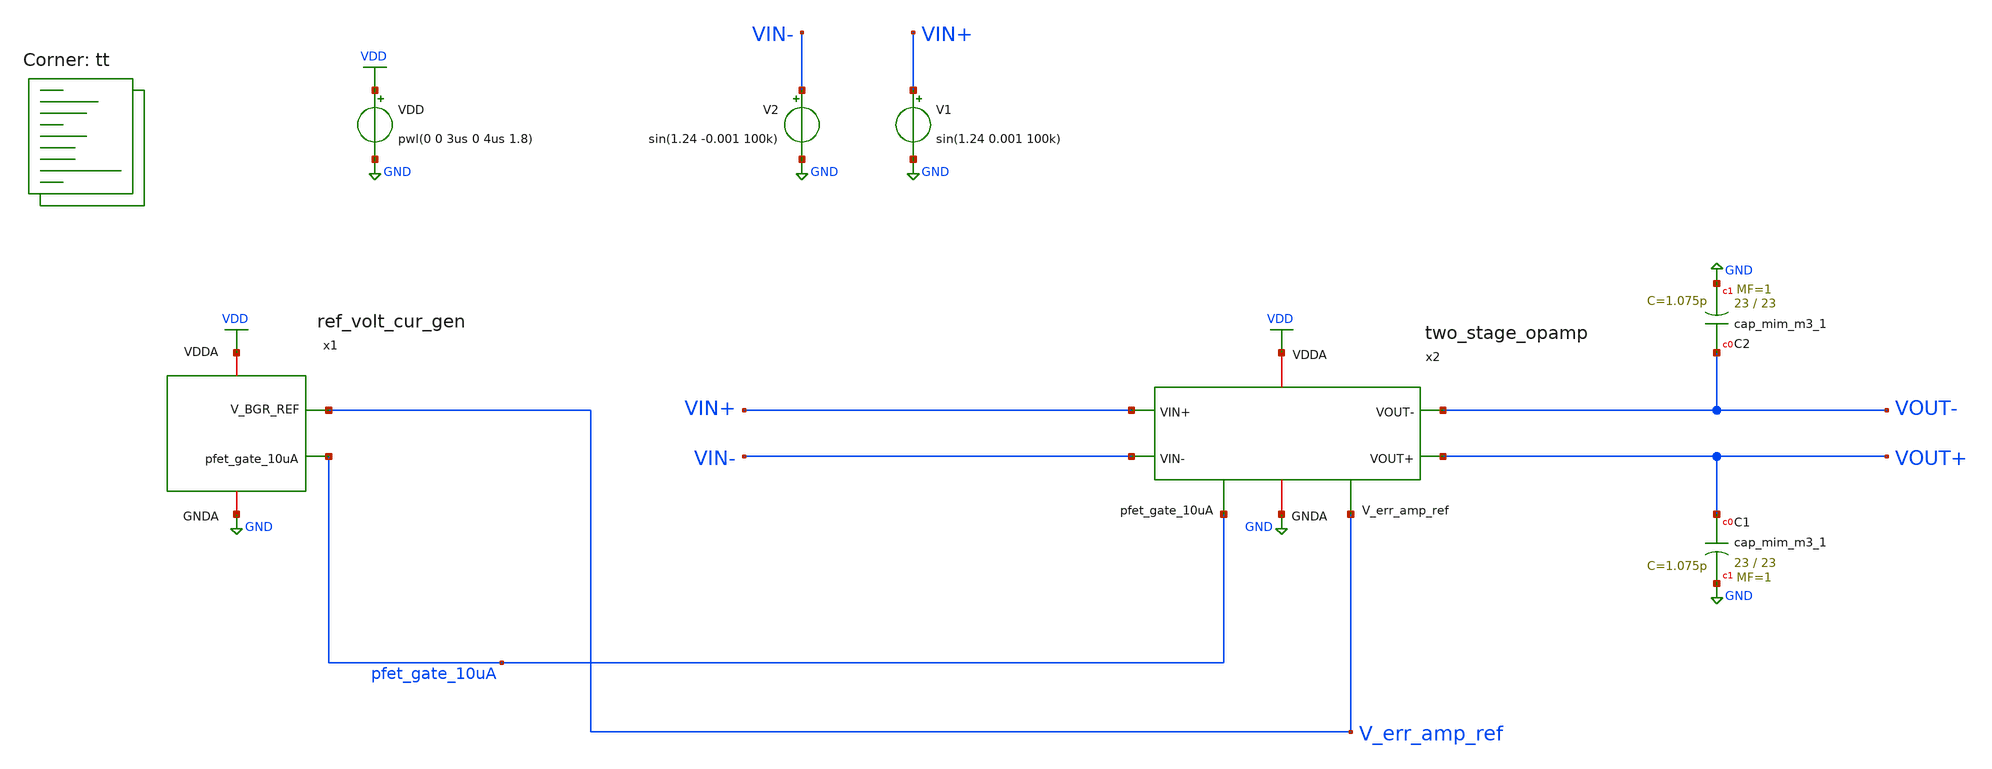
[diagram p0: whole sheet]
** sch_path: projects/opamp/xschem_ngspice/tb_opamp_full_6.sch
**.subckt tb_opamp_full_6
VDD VDD GND pwl(0 0 3us 0 4us 1.8)
V2 VIN- GND sin(1.24 -0.001 100k)
V1 VIN+ GND sin(1.24 0.001 100k)
x1 VDD V_err_amp_ref pfet_gate_10uA GND ref_volt_cur_gen
x2 VDD VOUT+ VOUT- pfet_gate_10uA V_err_amp_ref VIN+ VIN- GND two_stage_opamp
XC1 VOUT+ GND sky130_fd_pr__cap_mim_m3_1 W=23 L=23 MF=1 m=1
XC2 VOUT- GND sky130_fd_pr__cap_mim_m3_1 W=23 L=23 MF=1 m=1
**** begin user architecture code
.lib $::SKYWATER_MODELS/sky130.lib.spice tt




.option method=gear
.option wnflag=1
.option savecurrents

.save @m.x1.xm1.msky130_fd_pr__pfet_01v8[gm] @m.x1.xm1.msky130_fd_pr__pfet_01v8[vth] @m.x1.xm2.msky130_fd_pr__pfet_01v8[gm] @m.x1.xm2.msky130_fd_pr__pfet_01v8[vth] @m.x1.xm3.msky130_fd_pr__pfet_01v8[gm] @m.x1.xm3.msky130_fd_pr__pfet_01v8[vth] @m.x1.xm4.msky130_fd_pr__pfet_01v8[gm] @m.x1.xm4.msky130_fd_pr__pfet_01v8[vth] @m.x1.xm5.msky130_fd_pr__nfet_01v8[gm] @m.x1.xm5.msky130_fd_pr__nfet_01v8[vth] @m.x1.xm6.msky130_fd_pr__pfet_01v8[gm] @m.x1.xm6.msky130_fd_pr__pfet_01v8[vth] @m.x1.xm7.msky130_fd_pr__nfet_01v8[gm] @m.x1.xm7.msky130_fd_pr__nfet_01v8[vth] @m.x1.xm8.msky130_fd_pr__pfet_01v8[gm] @m.x1.xm8.msky130_fd_pr__pfet_01v8[vth] @m.x2.xm2.msky130_fd_pr__nfet_01v8[gm] @m.x2.xm2.msky130_fd_pr__nfet_01v8[vth] @m.x2.xm3.msky130_fd_pr__nfet_01v8[gm] @m.x2.xm3.msky130_fd_pr__nfet_01v8[vth] @m.x2.xm7.msky130_fd_pr__pfet_01v8[gm] @m.x2.xm7.msky130_fd_pr__pfet_01v8[vth] @m.x1.x1.xm1.msky130_fd_pr__nfet_01v8[gm] @m.x1.x1.xm2.msky130_fd_pr__nfet_01v8[gm] @m.x1.x1.xm3.msky130_fd_pr__nfet_01v8[gm] @m.x1.x1.xm4.msky130_fd_pr__nfet_01v8[gm] @m.x1.x1.xm5.msky130_fd_pr__pfet_01v8[gm] @m.x1.x1.xm6.msky130_fd_pr__nfet_01v8[gm] @m.x1.x1.xm7.msky130_fd_pr__pfet_01v8[gm] @m.x1.x2.xm1.msky130_fd_pr__nfet_01v8[gm] @m.x1.x2.xm2.msky130_fd_pr__nfet_01v8[gm] @m.x1.x2.xm3.msky130_fd_pr__nfet_01v8[gm] @m.x1.x2.xm4.msky130_fd_pr__nfet_01v8[gm] @m.x1.x2.xm5.msky130_fd_pr__pfet_01v8[gm] @m.x1.x2.xm6.msky130_fd_pr__nfet_01v8[gm] @m.x1.x2.xm7.msky130_fd_pr__pfet_01v8[gm] @m.x2.xm39.msky130_fd_pr__pfet_01v8[gm] @m.x2.xm39.msky130_fd_pr__pfet_01v8[vth] @m.x2.xm40.msky130_fd_pr__pfet_01v8[gm] @m.x2.xm40.msky130_fd_pr__pfet_01v8[vth]

* .ic v(v_top) = 1.8

.control

  * let runs=3
  * let run=1

  * dowhile run <= runs
    * save v(vout+) v(vout-) v(vin+) v(vin-) v(v_err_amp_ref) v(x2.x) v(x2.y) v(x2.vb1) v(x2.vb2)
+ v(x2.vb3) v(x2.v_tot)
    save all
    remzerovec
    set appendwrite
    * dc temp -40 120 10 VDD 0 4.0 0.2
    * dc VDD 0 2.0 0.02 temp -40 120 40
    * dc V5 0 0.01 0.0001
    tran 2n 30u
    * tran 1p 3n
    * tran 0.1ns 30us
    * ac dec 40 1 10T
    write tb_opamp_full_6.raw
    * write tb_opamp_full_6_mc.raw
    * write tb_opamp_full_6_tt_mm.raw
    * write tb_opamp_full_6_AC.raw
    * reset
    * let run = run + 1
  * end
.endc




**** end user architecture code
**.ends

* expanding   symbol:  ref_volt_cur_gen.sym # of pins=4
** sym_path: projects/opamp/xschem_ngspice/ref_volt_cur_gen.sym
** sch_path: projects/opamp/xschem_ngspice/ref_volt_cur_gen.sch
.subckt ref_volt_cur_gen VDDA V_BGR_REF pfet_gate_10uA GNDA
*.opin pfet_gate_10uA
*.iopin GNDA
*.opin V_BGR_REF
*.iopin VDDA
XM3 V_BGR_REF V_TOP VDDA VDDA sky130_fd_pr__pfet_01v8 L=0.5 W=10 nf=1 ad='int((nf+1)/2) * W/nf * 0.29'
+ as='int((nf+2)/2) * W/nf * 0.29' pd='2*int((nf+1)/2) * (W/nf + 0.29)' ps='2*int((nf+2)/2) * (W/nf + 0.29)'
+ nrd='0.29 / W' nrs='0.29 / W' sa=0 sb=0 sd=0 mult=1 m=1
XR4 GNDA V_BGR_REF GNDA sky130_fd_pr__res_xhigh_po_0p35 L=12.7 mult=1 m=1
XR5 GNDA V_CUR_REF_REG GNDA sky130_fd_pr__res_xhigh_po_0p35 L=12 mult=1 m=1
XM8 V_CUR_REF_REG pfet_gate_10uA VDDA VDDA sky130_fd_pr__pfet_01v8 L=0.5 W=1 nf=1 ad='int((nf+1)/2) * W/nf * 0.29'
+ as='int((nf+2)/2) * W/nf * 0.29' pd='2*int((nf+1)/2) * (W/nf + 0.29)' ps='2*int((nf+2)/2) * (W/nf + 0.29)'
+ nrd='0.29 / W' nrs='0.29 / W' sa=0 sb=0 sd=0 mult=1 m=1
XC1 VDDA V_TOP sky130_fd_pr__cap_mim_m3_1 W=10 L=10 MF=1 m=1
XQ1 GNDA GNDA Vin- sky130_fd_pr__pnp_05v5_W3p40L3p40 m=1
XQ2 GNDA GNDA Vbe2 sky130_fd_pr__pnp_05v5_W3p40L3p40 m=8
XM1 Vin- V_TOP VDDA VDDA sky130_fd_pr__pfet_01v8 L=0.5 W=10 nf=1 ad='int((nf+1)/2) * W/nf * 0.29' as='int((nf+2)/2) * W/nf * 0.29'
+ pd='2*int((nf+1)/2) * (W/nf + 0.29)' ps='2*int((nf+2)/2) * (W/nf + 0.29)' nrd='0.29 / W' nrs='0.29 / W'
+ sa=0 sb=0 sd=0 mult=1 m=1
XM2 Vin+ V_TOP VDDA VDDA sky130_fd_pr__pfet_01v8 L=0.5 W=10 nf=1 ad='int((nf+1)/2) * W/nf * 0.29' as='int((nf+2)/2) * W/nf * 0.29'
+ pd='2*int((nf+1)/2) * (W/nf + 0.29)' ps='2*int((nf+2)/2) * (W/nf + 0.29)' nrd='0.29 / W' nrs='0.29 / W'
+ sa=0 sb=0 sd=0 mult=1 m=1
XR1 Vbe2 Vin+ GNDA sky130_fd_pr__res_xhigh_po_0p35 L=2.3 mult=1 m=1
XR3 GNDA Vin+ GNDA sky130_fd_pr__res_xhigh_po_0p35 L=18 mult=1 m=1
XR2 GNDA Vin- GNDA sky130_fd_pr__res_xhigh_po_0p35 L=18 mult=1 m=1
XM6 start_up start_up start_up_nfet1 start_up_nfet1 sky130_fd_pr__nfet_01v8 L=10 W=1 nf=1 ad='int((nf+1)/2) * W/nf * 0.29'
+ as='int((nf+2)/2) * W/nf * 0.29' pd='2*int((nf+1)/2) * (W/nf + 0.29)' ps='2*int((nf+2)/2) * (W/nf + 0.29)'
+ nrd='0.29 / W' nrs='0.29 / W' sa=0 sb=0 sd=0 mult=1 m=1
XM4 start_up V_TOP VDDA VDDA sky130_fd_pr__pfet_01v8 L=0.5 W=10 nf=1 ad='int((nf+1)/2) * W/nf * 0.29'
+ as='int((nf+2)/2) * W/nf * 0.29' pd='2*int((nf+1)/2) * (W/nf + 0.29)' ps='2*int((nf+2)/2) * (W/nf + 0.29)'
+ nrd='0.29 / W' nrs='0.29 / W' sa=0 sb=0 sd=0 mult=1 m=1
XM5 Vin- start_up V_TOP VDDA sky130_fd_pr__pfet_01v8 L=0.15 W=2 nf=1 ad='int((nf+1)/2) * W/nf * 0.29'
+ as='int((nf+2)/2) * W/nf * 0.29' pd='2*int((nf+1)/2) * (W/nf + 0.29)' ps='2*int((nf+2)/2) * (W/nf + 0.29)'
+ nrd='0.29 / W' nrs='0.29 / W' sa=0 sb=0 sd=0 mult=1 m=1
XM7 start_up_nfet1 start_up_nfet1 GNDA GNDA sky130_fd_pr__nfet_01v8 L=10 W=1 nf=1 ad='int((nf+1)/2) * W/nf * 0.29'
+ as='int((nf+2)/2) * W/nf * 0.29' pd='2*int((nf+1)/2) * (W/nf + 0.29)' ps='2*int((nf+2)/2) * (W/nf + 0.29)'
+ nrd='0.29 / W' nrs='0.29 / W' sa=0 sb=0 sd=0 mult=1 m=1
x1 VDDA V_TOP Vin- Vin+ GNDA opamp_bandgap_2
x2 VDDA pfet_gate_10uA V_BGR_REF V_CUR_REF_REG GNDA opamp_bandgap_2
.ends


* expanding   symbol:  two_stage_opamp.sym # of pins=8
** sym_path: projects/opamp/xschem_ngspice/two_stage_opamp.sym
** sch_path: projects/opamp/xschem_ngspice/two_stage_opamp.sch
.subckt two_stage_opamp VDDA VOUT+ VOUT- pfet_gate_10uA V_err_amp_ref VIN+ VIN- GNDA
*.iopin VDDA
*.ipin V_err_amp_ref
*.iopin GNDA
*.ipin VIN-
*.ipin VIN+
*.ipin pfet_gate_10uA
*.opin VOUT+
*.opin VOUT-
XM7 VD1 VIN- V_p GNDA sky130_fd_pr__nfet_01v8 L=0.15 W=15 nf=1 ad='int((nf+1)/2) * W/nf * 0.29' as='int((nf+2)/2) * W/nf * 0.29'
+ pd='2*int((nf+1)/2) * (W/nf + 0.29)' ps='2*int((nf+2)/2) * (W/nf + 0.29)' nrd='0.29 / W' nrs='0.29 / W'
+ sa=0 sb=0 sd=0 mult=1 m=1
XM8 VD2 VIN+ V_p GNDA sky130_fd_pr__nfet_01v8 L=0.15 W=15 nf=1 ad='int((nf+1)/2) * W/nf * 0.29' as='int((nf+2)/2) * W/nf * 0.29'
+ pd='2*int((nf+1)/2) * (W/nf + 0.29)' ps='2*int((nf+2)/2) * (W/nf + 0.29)' nrd='0.29 / W' nrs='0.29 / W'
+ sa=0 sb=0 sd=0 mult=1 m=1
XM9 X Vb1 VD1 GNDA sky130_fd_pr__nfet_01v8 L=0.15 W=15 nf=1 ad='int((nf+1)/2) * W/nf * 0.29' as='int((nf+2)/2) * W/nf * 0.29'
+ pd='2*int((nf+1)/2) * (W/nf + 0.29)' ps='2*int((nf+2)/2) * (W/nf + 0.29)' nrd='0.29 / W' nrs='0.29 / W'
+ sa=0 sb=0 sd=0 mult=1 m=1
XM10 Y Vb1 VD2 GNDA sky130_fd_pr__nfet_01v8 L=0.15 W=15 nf=1 ad='int((nf+1)/2) * W/nf * 0.29' as='int((nf+2)/2) * W/nf * 0.29'
+ pd='2*int((nf+1)/2) * (W/nf + 0.29)' ps='2*int((nf+2)/2) * (W/nf + 0.29)' nrd='0.29 / W' nrs='0.29 / W'
+ sa=0 sb=0 sd=0 mult=1 m=1
XM11 X Vb2 VD7 VD7 sky130_fd_pr__pfet_01v8 L=0.2 W=35 nf=1 ad='int((nf+1)/2) * W/nf * 0.29' as='int((nf+2)/2) * W/nf * 0.29'
+ pd='2*int((nf+1)/2) * (W/nf + 0.29)' ps='2*int((nf+2)/2) * (W/nf + 0.29)' nrd='0.29 / W' nrs='0.29 / W'
+ sa=0 sb=0 sd=0 mult=1 m=1
XM12 Y Vb2 VD6 VD6 sky130_fd_pr__pfet_01v8 L=0.2 W=35 nf=1 ad='int((nf+1)/2) * W/nf * 0.29' as='int((nf+2)/2) * W/nf * 0.29'
+ pd='2*int((nf+1)/2) * (W/nf + 0.29)' ps='2*int((nf+2)/2) * (W/nf + 0.29)' nrd='0.29 / W' nrs='0.29 / W'
+ sa=0 sb=0 sd=0 mult=1 m=1
XM13 VD7 Vb3 VDDA VDDA sky130_fd_pr__pfet_01v8 L=0.2 W=35 nf=1 ad='int((nf+1)/2) * W/nf * 0.29' as='int((nf+2)/2) * W/nf * 0.29'
+ pd='2*int((nf+1)/2) * (W/nf + 0.29)' ps='2*int((nf+2)/2) * (W/nf + 0.29)' nrd='0.29 / W' nrs='0.29 / W'
+ sa=0 sb=0 sd=0 mult=1 m=1
XM14 VD6 Vb3 VDDA VDDA sky130_fd_pr__pfet_01v8 L=0.2 W=35 nf=1 ad='int((nf+1)/2) * W/nf * 0.29' as='int((nf+2)/2) * W/nf * 0.29'
+ pd='2*int((nf+1)/2) * (W/nf + 0.29)' ps='2*int((nf+2)/2) * (W/nf + 0.29)' nrd='0.29 / W' nrs='0.29 / W'
+ sa=0 sb=0 sd=0 mult=1 m=1
XM15 V_p VGS9 GNDA GNDA sky130_fd_pr__nfet_01v8 L=0.15 W=45 nf=1 ad='int((nf+1)/2) * W/nf * 0.29' as='int((nf+2)/2) * W/nf * 0.29'
+ pd='2*int((nf+1)/2) * (W/nf + 0.29)' ps='2*int((nf+2)/2) * (W/nf + 0.29)' nrd='0.29 / W' nrs='0.29 / W'
+ sa=0 sb=0 sd=0 mult=1 m=1
XM16 V_p_mir VGS9 GNDA GNDA sky130_fd_pr__nfet_01v8 L=0.15 W=5 nf=1 ad='int((nf+1)/2) * W/nf * 0.29'
+ as='int((nf+2)/2) * W/nf * 0.29' pd='2*int((nf+1)/2) * (W/nf + 0.29)' ps='2*int((nf+2)/2) * (W/nf + 0.29)'
+ nrd='0.29 / W' nrs='0.29 / W' sa=0 sb=0 sd=0 mult=1 m=1
XM17 VGS9 VIN+ V_p_mir GNDA sky130_fd_pr__nfet_01v8 L=0.15 W=1.5 nf=1 ad='int((nf+1)/2) * W/nf * 0.29'
+ as='int((nf+2)/2) * W/nf * 0.29' pd='2*int((nf+1)/2) * (W/nf + 0.29)' ps='2*int((nf+2)/2) * (W/nf + 0.29)'
+ nrd='0.29 / W' nrs='0.29 / W' sa=0 sb=0 sd=0 mult=1 m=1
XM18 VGS9 VIN- V_p_mir GNDA sky130_fd_pr__nfet_01v8 L=0.15 W=1.5 nf=1 ad='int((nf+1)/2) * W/nf * 0.29'
+ as='int((nf+2)/2) * W/nf * 0.29' pd='2*int((nf+1)/2) * (W/nf + 0.29)' ps='2*int((nf+2)/2) * (W/nf + 0.29)'
+ nrd='0.29 / W' nrs='0.29 / W' sa=0 sb=0 sd=0 mult=1 m=1
XM19 Vb1 Vb1 V_p GNDA sky130_fd_pr__nfet_01v8 L=1.9 W=1 nf=1 ad='int((nf+1)/2) * W/nf * 0.29' as='int((nf+2)/2) * W/nf * 0.29'
+ pd='2*int((nf+1)/2) * (W/nf + 0.29)' ps='2*int((nf+2)/2) * (W/nf + 0.29)' nrd='0.29 / W' nrs='0.29 / W'
+ sa=0 sb=0 sd=0 mult=1 m=1
XM25 VDDA X V_4 GNDA sky130_fd_pr__nfet_01v8 L=0.15 W=30 nf=1 ad='int((nf+1)/2) * W/nf * 0.29' as='int((nf+2)/2) * W/nf * 0.29'
+ pd='2*int((nf+1)/2) * (W/nf + 0.29)' ps='2*int((nf+2)/2) * (W/nf + 0.29)' nrd='0.29 / W' nrs='0.29 / W'
+ sa=0 sb=0 sd=0 mult=1 m=1
XM26 GNDA X V_3 VDDA sky130_fd_pr__pfet_01v8 L=0.15 W=20 nf=1 ad='int((nf+1)/2) * W/nf * 0.29' as='int((nf+2)/2) * W/nf * 0.29'
+ pd='2*int((nf+1)/2) * (W/nf + 0.29)' ps='2*int((nf+2)/2) * (W/nf + 0.29)' nrd='0.29 / W' nrs='0.29 / W'
+ sa=0 sb=0 sd=0 mult=1 m=1
XR10 V_3 V_tot GNDA sky130_fd_pr__res_xhigh_po_0p35 L=3.5 mult=1 m=1
XR11 V_4 V_tot GNDA sky130_fd_pr__res_xhigh_po_0p35 L=3.5 mult=1 m=1
XR12 V_1 V_tot GNDA sky130_fd_pr__res_xhigh_po_0p35 L=3.5 mult=1 m=1
XR13 V_2 V_tot GNDA sky130_fd_pr__res_xhigh_po_0p35 L=3.5 mult=1 m=1
XM27 VDDA Y V_2 GNDA sky130_fd_pr__nfet_01v8 L=0.15 W=30 nf=1 ad='int((nf+1)/2) * W/nf * 0.29' as='int((nf+2)/2) * W/nf * 0.29'
+ pd='2*int((nf+1)/2) * (W/nf + 0.29)' ps='2*int((nf+2)/2) * (W/nf + 0.29)' nrd='0.29 / W' nrs='0.29 / W'
+ sa=0 sb=0 sd=0 mult=1 m=1
XM28 GNDA Y V_1 VDDA sky130_fd_pr__pfet_01v8 L=0.15 W=20 nf=1 ad='int((nf+1)/2) * W/nf * 0.29' as='int((nf+2)/2) * W/nf * 0.29'
+ pd='2*int((nf+1)/2) * (W/nf + 0.29)' ps='2*int((nf+2)/2) * (W/nf + 0.29)' nrd='0.29 / W' nrs='0.29 / W'
+ sa=0 sb=0 sd=0 mult=1 m=1
XM29 err_opamp_mir V_tot V_err_p VDDA sky130_fd_pr__pfet_01v8 L=0.15 W=2.5 nf=1 ad='int((nf+1)/2) * W/nf * 0.29'
+ as='int((nf+2)/2) * W/nf * 0.29' pd='2*int((nf+1)/2) * (W/nf + 0.29)' ps='2*int((nf+2)/2) * (W/nf + 0.29)'
+ nrd='0.29 / W' nrs='0.29 / W' sa=0 sb=0 sd=0 mult=1 m=1
XM30 err_opamp_out V_err_amp_ref V_err_p VDDA sky130_fd_pr__pfet_01v8 L=0.15 W=2.5 nf=1 ad='int((nf+1)/2) * W/nf * 0.29'
+ as='int((nf+2)/2) * W/nf * 0.29' pd='2*int((nf+1)/2) * (W/nf + 0.29)' ps='2*int((nf+2)/2) * (W/nf + 0.29)'
+ nrd='0.29 / W' nrs='0.29 / W' sa=0 sb=0 sd=0 mult=1 m=1
XM31 err_opamp_mir err_opamp_mir GNDA GNDA sky130_fd_pr__nfet_01v8 L=0.15 W=2.5 nf=1 ad='int((nf+1)/2) * W/nf * 0.29'
+ as='int((nf+2)/2) * W/nf * 0.29' pd='2*int((nf+1)/2) * (W/nf + 0.29)' ps='2*int((nf+2)/2) * (W/nf + 0.29)'
+ nrd='0.29 / W' nrs='0.29 / W' sa=0 sb=0 sd=0 mult=1 m=1
XM32 err_opamp_out err_opamp_mir GNDA GNDA sky130_fd_pr__nfet_01v8 L=0.15 W=2.5 nf=1 ad='int((nf+1)/2) * W/nf * 0.29'
+ as='int((nf+2)/2) * W/nf * 0.29' pd='2*int((nf+1)/2) * (W/nf + 0.29)' ps='2*int((nf+2)/2) * (W/nf + 0.29)'
+ nrd='0.29 / W' nrs='0.29 / W' sa=0 sb=0 sd=0 mult=1 m=1
XM33 V_err_p V_gate VDDA VDDA sky130_fd_pr__pfet_01v8 L=0.15 W=5.0 nf=2 ad='int((nf+1)/2) * W/nf * 0.29'
+ as='int((nf+2)/2) * W/nf * 0.29' pd='2*int((nf+1)/2) * (W/nf + 0.29)' ps='2*int((nf+2)/2) * (W/nf + 0.29)'
+ nrd='0.29 / W' nrs='0.29 / W' sa=0 sb=0 sd=0 mult=1 m=1
XM34 V_gate V_tot V_err_mir_p VDDA sky130_fd_pr__pfet_01v8 L=0.15 W=2.5 nf=1 ad='int((nf+1)/2) * W/nf * 0.29'
+ as='int((nf+2)/2) * W/nf * 0.29' pd='2*int((nf+1)/2) * (W/nf + 0.29)' ps='2*int((nf+2)/2) * (W/nf + 0.29)'
+ nrd='0.29 / W' nrs='0.29 / W' sa=0 sb=0 sd=0 mult=1 m=1
XM35 V_gate V_err_amp_ref V_err_mir_p VDDA sky130_fd_pr__pfet_01v8 L=0.15 W=2.5 nf=1 ad='int((nf+1)/2) * W/nf * 0.29'
+ as='int((nf+2)/2) * W/nf * 0.29' pd='2*int((nf+1)/2) * (W/nf + 0.29)' ps='2*int((nf+2)/2) * (W/nf + 0.29)'
+ nrd='0.29 / W' nrs='0.29 / W' sa=0 sb=0 sd=0 mult=1 m=1
XM36 V_err_mir_p V_gate VDDA VDDA sky130_fd_pr__pfet_01v8 L=0.15 W=5.0 nf=2 ad='int((nf+1)/2) * W/nf * 0.29'
+ as='int((nf+2)/2) * W/nf * 0.29' pd='2*int((nf+1)/2) * (W/nf + 0.29)' ps='2*int((nf+2)/2) * (W/nf + 0.29)'
+ nrd='0.29 / W' nrs='0.29 / W' sa=0 sb=0 sd=0 mult=1 m=1
XM37 VOUT- V_b GNDA GNDA sky130_fd_pr__nfet_01v8 L=0.6 W=28 nf=1 ad='int((nf+1)/2) * W/nf * 0.29' as='int((nf+2)/2) * W/nf * 0.29'
+ pd='2*int((nf+1)/2) * (W/nf + 0.29)' ps='2*int((nf+2)/2) * (W/nf + 0.29)' nrd='0.29 / W' nrs='0.29 / W'
+ sa=0 sb=0 sd=0 mult=1 m=1
XM38 VOUT+ V_b GNDA GNDA sky130_fd_pr__nfet_01v8 L=0.6 W=28 nf=1 ad='int((nf+1)/2) * W/nf * 0.29' as='int((nf+2)/2) * W/nf * 0.29'
+ pd='2*int((nf+1)/2) * (W/nf + 0.29)' ps='2*int((nf+2)/2) * (W/nf + 0.29)' nrd='0.29 / W' nrs='0.29 / W'
+ sa=0 sb=0 sd=0 mult=1 m=1
XM39 VOUT- X VDDA VDDA sky130_fd_pr__pfet_01v8 L=0.15 W=59 nf=1 ad='int((nf+1)/2) * W/nf * 0.29' as='int((nf+2)/2) * W/nf * 0.29'
+ pd='2*int((nf+1)/2) * (W/nf + 0.29)' ps='2*int((nf+2)/2) * (W/nf + 0.29)' nrd='0.29 / W' nrs='0.29 / W'
+ sa=0 sb=0 sd=0 mult=1 m=1
XM40 VOUT+ Y VDDA VDDA sky130_fd_pr__pfet_01v8 L=0.15 W=59 nf=1 ad='int((nf+1)/2) * W/nf * 0.29' as='int((nf+2)/2) * W/nf * 0.29'
+ pd='2*int((nf+1)/2) * (W/nf + 0.29)' ps='2*int((nf+2)/2) * (W/nf + 0.29)' nrd='0.29 / W' nrs='0.29 / W'
+ sa=0 sb=0 sd=0 mult=1 m=1
XR22 VOUT- V_b GNDA sky130_fd_pr__res_xhigh_po_0p35 L=5.25 mult=1 m=1
XR23 VOUT+ V_b GNDA sky130_fd_pr__res_xhigh_po_0p35 L=5.25 mult=1 m=1
XM41 V_p err_opamp_out GNDA GNDA sky130_fd_pr__nfet_01v8 L=0.15 W=2.5 nf=1 ad='int((nf+1)/2) * W/nf * 0.29'
+ as='int((nf+2)/2) * W/nf * 0.29' pd='2*int((nf+1)/2) * (W/nf + 0.29)' ps='2*int((nf+2)/2) * (W/nf + 0.29)'
+ nrd='0.29 / W' nrs='0.29 / W' sa=0 sb=0 sd=0 mult=1 m=1
XM5 Vb2 Vb2 VDDA VDDA sky130_fd_pr__pfet_01v8 L=0.2 W=0.63 nf=1 ad='int((nf+1)/2) * W/nf * 0.29' as='int((nf+2)/2) * W/nf * 0.29'
+ pd='2*int((nf+1)/2) * (W/nf + 0.29)' ps='2*int((nf+2)/2) * (W/nf + 0.29)' nrd='0.29 / W' nrs='0.29 / W'
+ sa=0 sb=0 sd=0 mult=1 m=1
XM6 Vb3 Vb2 V5 V5 sky130_fd_pr__pfet_01v8 L=0.2 W=3.5 nf=1 ad='int((nf+1)/2) * W/nf * 0.29' as='int((nf+2)/2) * W/nf * 0.29'
+ pd='2*int((nf+1)/2) * (W/nf + 0.29)' ps='2*int((nf+2)/2) * (W/nf + 0.29)' nrd='0.29 / W' nrs='0.29 / W'
+ sa=0 sb=0 sd=0 mult=1 m=1
XM43 V5 Vb3 VDDA VDDA sky130_fd_pr__pfet_01v8 L=0.2 W=3.2 nf=1 ad='int((nf+1)/2) * W/nf * 0.29' as='int((nf+2)/2) * W/nf * 0.29'
+ pd='2*int((nf+1)/2) * (W/nf + 0.29)' ps='2*int((nf+2)/2) * (W/nf + 0.29)' nrd='0.29 / W' nrs='0.29 / W'
+ sa=0 sb=0 sd=0 mult=1 m=1
XM42 nfet_gate_10uA pfet_gate_10uA VDDA VDDA sky130_fd_pr__pfet_01v8 L=0.5 W=1 nf=1 ad='int((nf+1)/2) * W/nf * 0.29'
+ as='int((nf+2)/2) * W/nf * 0.29' pd='2*int((nf+1)/2) * (W/nf + 0.29)' ps='2*int((nf+2)/2) * (W/nf + 0.29)'
+ nrd='0.29 / W' nrs='0.29 / W' sa=0 sb=0 sd=0 mult=1 m=1
XM44 Vb2 nfet_gate_10uA GNDA GNDA sky130_fd_pr__nfet_01v8 L=0.5 W=1 nf=1 ad='int((nf+1)/2) * W/nf * 0.29'
+ as='int((nf+2)/2) * W/nf * 0.29' pd='2*int((nf+1)/2) * (W/nf + 0.29)' ps='2*int((nf+2)/2) * (W/nf + 0.29)'
+ nrd='0.29 / W' nrs='0.29 / W' sa=0 sb=0 sd=0 mult=6 m=6
XM45 Vb3 nfet_gate_10uA GNDA GNDA sky130_fd_pr__nfet_01v8 L=0.5 W=1 nf=1 ad='int((nf+1)/2) * W/nf * 0.29'
+ as='int((nf+2)/2) * W/nf * 0.29' pd='2*int((nf+1)/2) * (W/nf + 0.29)' ps='2*int((nf+2)/2) * (W/nf + 0.29)'
+ nrd='0.29 / W' nrs='0.29 / W' sa=0 sb=0 sd=0 mult=5 m=5
XM50 Vb1 pfet_gate_10uA VDDA VDDA sky130_fd_pr__pfet_01v8 L=0.5 W=1 nf=1 ad='int((nf+1)/2) * W/nf * 0.29'
+ as='int((nf+2)/2) * W/nf * 0.29' pd='2*int((nf+1)/2) * (W/nf + 0.29)' ps='2*int((nf+2)/2) * (W/nf + 0.29)'
+ nrd='0.29 / W' nrs='0.29 / W' sa=0 sb=0 sd=0 mult=3 m=3
XM51 VGS9 pfet_gate_10uA VDDA VDDA sky130_fd_pr__pfet_01v8 L=0.5 W=1 nf=1 ad='int((nf+1)/2) * W/nf * 0.29'
+ as='int((nf+2)/2) * W/nf * 0.29' pd='2*int((nf+1)/2) * (W/nf + 0.29)' ps='2*int((nf+2)/2) * (W/nf + 0.29)'
+ nrd='0.29 / W' nrs='0.29 / W' sa=0 sb=0 sd=0 mult=9 m=9
XM53 V_gate nfet_gate_10uA GNDA GNDA sky130_fd_pr__nfet_01v8 L=0.5 W=1 nf=1 ad='int((nf+1)/2) * W/nf * 0.29'
+ as='int((nf+2)/2) * W/nf * 0.29' pd='2*int((nf+1)/2) * (W/nf + 0.29)' ps='2*int((nf+2)/2) * (W/nf + 0.29)'
+ nrd='0.29 / W' nrs='0.29 / W' sa=0 sb=0 sd=0 mult=2 m=2
XM54 V_4 nfet_gate_10uA GNDA GNDA sky130_fd_pr__nfet_01v8 L=0.5 W=1 nf=1 ad='int((nf+1)/2) * W/nf * 0.29'
+ as='int((nf+2)/2) * W/nf * 0.29' pd='2*int((nf+1)/2) * (W/nf + 0.29)' ps='2*int((nf+2)/2) * (W/nf + 0.29)'
+ nrd='0.29 / W' nrs='0.29 / W' sa=0 sb=0 sd=0 mult=3 m=3
XM55 V_2 nfet_gate_10uA GNDA GNDA sky130_fd_pr__nfet_01v8 L=0.5 W=1 nf=1 ad='int((nf+1)/2) * W/nf * 0.29'
+ as='int((nf+2)/2) * W/nf * 0.29' pd='2*int((nf+1)/2) * (W/nf + 0.29)' ps='2*int((nf+2)/2) * (W/nf + 0.29)'
+ nrd='0.29 / W' nrs='0.29 / W' sa=0 sb=0 sd=0 mult=3 m=3
XM56 V_3 pfet_gate_10uA VDDA VDDA sky130_fd_pr__pfet_01v8 L=0.5 W=1 nf=1 ad='int((nf+1)/2) * W/nf * 0.29'
+ as='int((nf+2)/2) * W/nf * 0.29' pd='2*int((nf+1)/2) * (W/nf + 0.29)' ps='2*int((nf+2)/2) * (W/nf + 0.29)'
+ nrd='0.29 / W' nrs='0.29 / W' sa=0 sb=0 sd=0 mult=4 m=4
XM57 V_1 pfet_gate_10uA VDDA VDDA sky130_fd_pr__pfet_01v8 L=0.5 W=1 nf=1 ad='int((nf+1)/2) * W/nf * 0.29'
+ as='int((nf+2)/2) * W/nf * 0.29' pd='2*int((nf+1)/2) * (W/nf + 0.29)' ps='2*int((nf+2)/2) * (W/nf + 0.29)'
+ nrd='0.29 / W' nrs='0.29 / W' sa=0 sb=0 sd=0 mult=4 m=4
XM20 nfet_gate_10uA nfet_gate_10uA GNDA GNDA sky130_fd_pr__nfet_01v8 L=0.5 W=1 nf=1 ad='int((nf+1)/2) * W/nf * 0.29'
+ as='int((nf+2)/2) * W/nf * 0.29' pd='2*int((nf+1)/2) * (W/nf + 0.29)' ps='2*int((nf+2)/2) * (W/nf + 0.29)'
+ nrd='0.29 / W' nrs='0.29 / W' sa=0 sb=0 sd=0 mult=1 m=1
XC6 Y net1 sky130_fd_pr__cap_mim_m3_1 W=25 L=25 MF=1 m=1
XC7 X net2 sky130_fd_pr__cap_mim_m3_1 W=25 L=25 MF=1 m=1
XR29 net2 VOUT- GND sky130_fd_pr__res_high_po W=1.19 L=1 mult=1 m=1
XR32 net1 VOUT+ GND sky130_fd_pr__res_high_po W=1.19 L=1 mult=1 m=1
.ends


* expanding   symbol:
*+  /foss/designs/projects/bandgapref/xschem_ngspice/new_files/opamp_bandgap_2.sym # of pins=5
** sym_path: projects/bandgapref/xschem_ngspice/new_files/opamp_bandgap_2.sym
** sch_path: projects/bandgapref/xschem_ngspice/new_files/opamp_bandgap_2.sch
.subckt opamp_bandgap_2 VDDA Vout Vin- Vin+ GNDA
*.ipin Vin+
*.opin Vout
*.ipin Vin-
*.ipin GNDA
*.ipin VDDA
XM1 V_p VDDA GNDA GNDA sky130_fd_pr__nfet_01v8 L=5 W=2.5 nf=1 ad='int((nf+1)/2) * W/nf * 0.29' as='int((nf+2)/2) * W/nf * 0.29'
+ pd='2*int((nf+1)/2) * (W/nf + 0.29)' ps='2*int((nf+2)/2) * (W/nf + 0.29)' nrd='0.29 / W' nrs='0.29 / W'
+ sa=0 sb=0 sd=0 mult=1 m=1
XM2 V_mirror Vin- V_p GNDA sky130_fd_pr__nfet_01v8 L=0.2 W=2.5 nf=1 ad='int((nf+1)/2) * W/nf * 0.29'
+ as='int((nf+2)/2) * W/nf * 0.29' pd='2*int((nf+1)/2) * (W/nf + 0.29)' ps='2*int((nf+2)/2) * (W/nf + 0.29)'
+ nrd='0.29 / W' nrs='0.29 / W' sa=0 sb=0 sd=0 mult=1 m=1
XM3 1st_Vout Vin+ V_p GNDA sky130_fd_pr__nfet_01v8 L=0.2 W=2.5 nf=1 ad='int((nf+1)/2) * W/nf * 0.29'
+ as='int((nf+2)/2) * W/nf * 0.29' pd='2*int((nf+1)/2) * (W/nf + 0.29)' ps='2*int((nf+2)/2) * (W/nf + 0.29)'
+ nrd='0.29 / W' nrs='0.29 / W' sa=0 sb=0 sd=0 mult=1 m=1
XM5 V_mirror V_mirror VDDA VDDA sky130_fd_pr__pfet_01v8 L=0.2 W=6 nf=2 ad='int((nf+1)/2) * W/nf * 0.29'
+ as='int((nf+2)/2) * W/nf * 0.29' pd='2*int((nf+1)/2) * (W/nf + 0.29)' ps='2*int((nf+2)/2) * (W/nf + 0.29)'
+ nrd='0.29 / W' nrs='0.29 / W' sa=0 sb=0 sd=0 mult=1 m=1
XM6 1st_Vout V_mirror VDDA VDDA sky130_fd_pr__pfet_01v8 L=0.2 W=6 nf=2 ad='int((nf+1)/2) * W/nf * 0.29'
+ as='int((nf+2)/2) * W/nf * 0.29' pd='2*int((nf+1)/2) * (W/nf + 0.29)' ps='2*int((nf+2)/2) * (W/nf + 0.29)'
+ nrd='0.29 / W' nrs='0.29 / W' sa=0 sb=0 sd=0 mult=1 m=1
XM4 Vout VDDA GNDA GNDA sky130_fd_pr__nfet_01v8 L=5 W=2.5 nf=1 ad='int((nf+1)/2) * W/nf * 0.29' as='int((nf+2)/2) * W/nf * 0.29'
+ pd='2*int((nf+1)/2) * (W/nf + 0.29)' ps='2*int((nf+2)/2) * (W/nf + 0.29)' nrd='0.29 / W' nrs='0.29 / W'
+ sa=0 sb=0 sd=0 mult=1 m=1
XM7 Vout 1st_Vout VDDA VDDA sky130_fd_pr__pfet_01v8 L=0.2 W=6 nf=2 ad='int((nf+1)/2) * W/nf * 0.29' as='int((nf+2)/2) * W/nf * 0.29'
+ pd='2*int((nf+1)/2) * (W/nf + 0.29)' ps='2*int((nf+2)/2) * (W/nf + 0.29)' nrd='0.29 / W' nrs='0.29 / W'
+ sa=0 sb=0 sd=0 mult=1 m=1
XC1 1st_Vout cap_res sky130_fd_pr__cap_mim_m3_1 W=2 L=2 MF=20 m=20
XM8 Vout VDDA VDDA VDDA sky130_fd_pr__pfet_01v8 L=0.2 W=2 nf=2 ad='int((nf+1)/2) * W/nf * 0.29' as='int((nf+2)/2) * W/nf * 0.29'
+ pd='2*int((nf+1)/2) * (W/nf + 0.29)' ps='2*int((nf+2)/2) * (W/nf + 0.29)' nrd='0.29 / W' nrs='0.29 / W'
+ sa=0 sb=0 sd=0 mult=1 m=1
XR2 Vout cap_res GNDA sky130_fd_pr__res_high_po_0p35 L=2.05 mult=1 m=1
.ends

.GLOBAL GND
.GLOBAL VDD
.end
